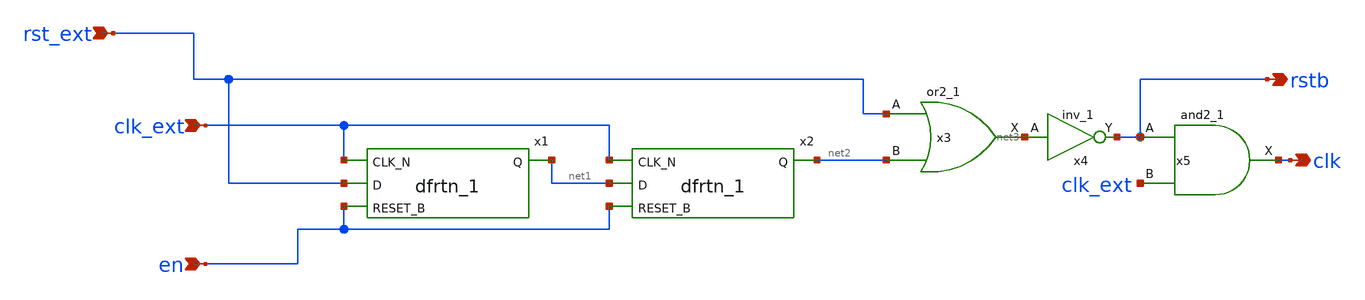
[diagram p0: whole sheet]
** sch_path: xschem/Clock Synchronizer/synchronizer.sch
**.subckt synchronizer rst_ext clk_ext en rstb clk
*.ipin rst_ext
*.ipin clk_ext
*.ipin en
*.opin rstb
*.opin clk
x1 clk_ext rst_ext en GND GND VDD VDD net1 sky130_fd_sc_lp__dfrtn_1
x3 rst_ext net2 GND GND VDD VDD net3 sky130_fd_sc_lp__or2_1
x4 net3 GND GND VDD VDD rstb sky130_fd_sc_lp__inv_1
x2 clk_ext net1 en GND GND VDD VDD net2 sky130_fd_sc_lp__dfrtn_1
x5 rstb clk_ext GND GND VDD VDD clk sky130_fd_sc_lp__and2_1
**.ends
.end
